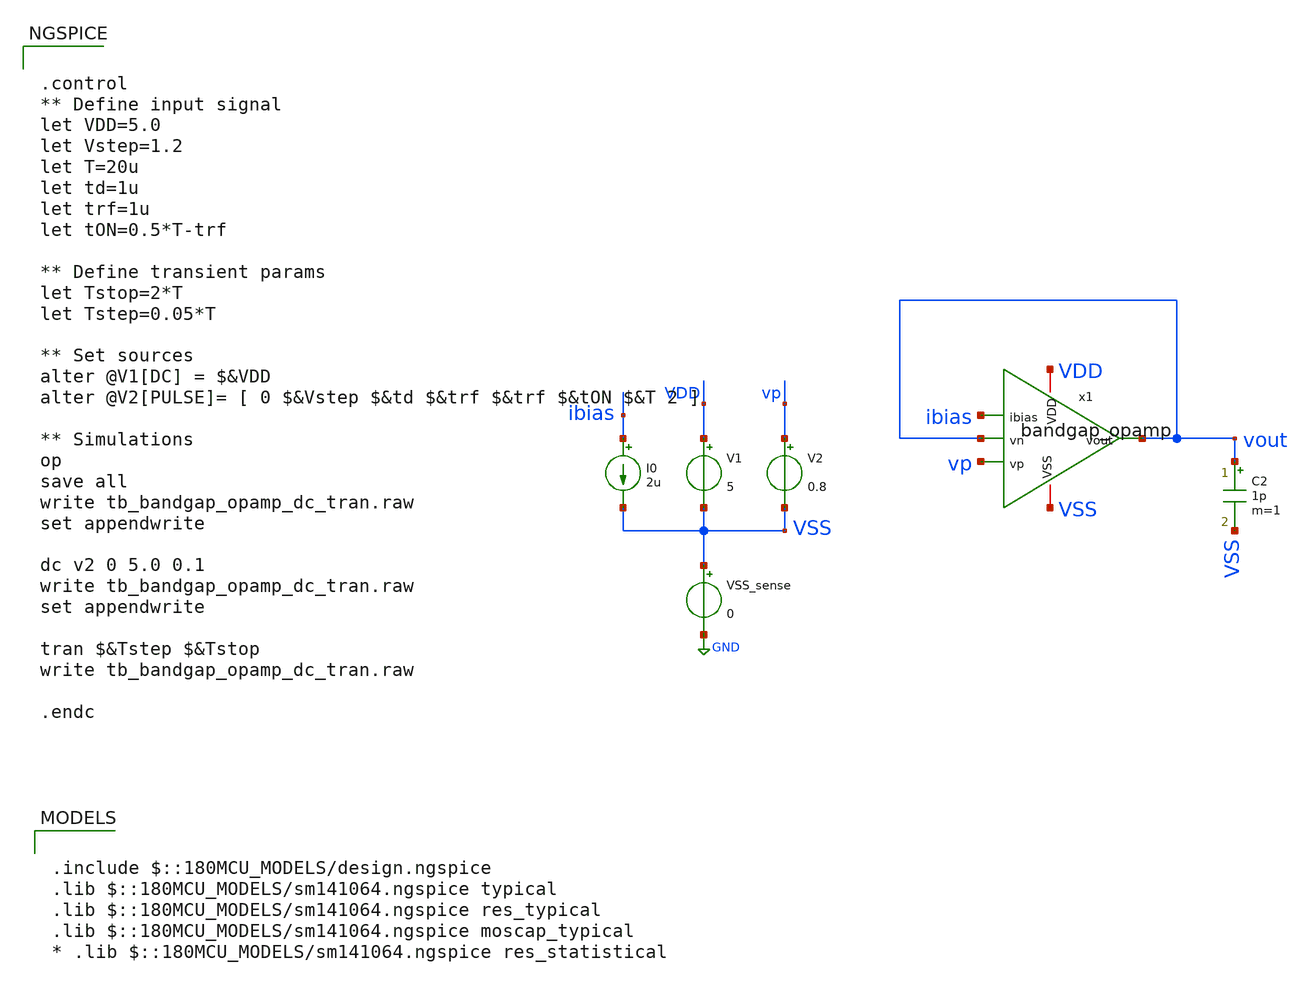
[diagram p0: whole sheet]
** sch_path: designs/libs/tb_bandgap/tb_bandgap_opamp_dc_tran/tb_bandgap_opamp_dc_tran.sch
**.subckt tb_bandgap_opamp_dc_tran
V1 VDD VSS 5
V2 vp VSS 0.8
VSS_sense VSS GND 0
C2 vout VSS 1p m=1
I0 ibias VSS 2u
x1 VDD ibias vout vp vout VSS bandgap_opamp
**** begin user architecture code

.include $::180MCU_MODELS/design.ngspice
.lib $::180MCU_MODELS/sm141064.ngspice typical
.lib $::180MCU_MODELS/sm141064.ngspice res_typical
.lib $::180MCU_MODELS/sm141064.ngspice moscap_typical
* .lib $::180MCU_MODELS/sm141064.ngspice res_statistical



.control
** Define input signal
let VDD=5.0
let Vstep=1.2
let T=20u
let td=1u
let trf=1u
let tON=0.5*T-trf

** Define transient params
let Tstop=2*T
let Tstep=0.05*T

** Set sources
alter @V1[DC] = $&VDD
alter @V2[PULSE]= [ 0 $&Vstep $&td $&trf $&trf $&tON $&T 2 ]

** Simulations
op
save all
write tb_bandgap_opamp_dc_tran.raw
set appendwrite

dc v2 0 5.0 0.1
write tb_bandgap_opamp_dc_tran.raw
set appendwrite

tran $&Tstep $&Tstop
write tb_bandgap_opamp_dc_tran.raw

.endc


**** end user architecture code
**.ends

* expanding   symbol:  libs/core_bandgap/bandgap_opamp/bandgap_opamp.sym # of pins=6
** sym_path: designs/libs/core_bandgap/bandgap_opamp/bandgap_opamp.sym
** sch_path: designs/libs/core_bandgap/bandgap_opamp/bandgap_opamp.sch
.subckt bandgap_opamp VDD ibias vn vp vout VSS
*.ipin vn
*.ipin vp
*.opin vout
*.ipin ibias
*.iopin VDD
*.iopin VSS
XC1 vout net3 cap_nmos_03v3_b c_width=15u c_length=15u m=1
XM9 ibias ibias VDD VDD pfet_05v0 L=1u W=1u nf=1 ad='int((nf+1)/2) * W/nf * 0.18u' as='int((nf+2)/2) * W/nf * 0.18u'
+ pd='2*int((nf+1)/2) * (W/nf + 0.18u)' ps='2*int((nf+2)/2) * (W/nf + 0.18u)' nrd='0.18u / W' nrs='0.18u / W'
+ sa=0 sb=0 sd=0 m=1
XM10 net2 net2 VSS VSS nfet_05v0 L=2u W=1u nf=1 ad='int((nf+1)/2) * W/nf * 0.18u' as='int((nf+2)/2) * W/nf * 0.18u'
+ pd='2*int((nf+1)/2) * (W/nf + 0.18u)' ps='2*int((nf+2)/2) * (W/nf + 0.18u)' nrd='0.18u / W' nrs='0.18u / W'
+ sa=0 sb=0 sd=0 m=1
XM3 net1 ibias VDD VDD pfet_05v0 L=1u W=1u nf=1 ad='int((nf+1)/2) * W/nf * 0.18u' as='int((nf+2)/2) * W/nf * 0.18u'
+ pd='2*int((nf+1)/2) * (W/nf + 0.18u)' ps='2*int((nf+2)/2) * (W/nf + 0.18u)' nrd='0.18u / W' nrs='0.18u / W'
+ sa=0 sb=0 sd=0 m=1
XM4 vout ibias VDD VDD pfet_05v0 L=1u W=1u nf=1 ad='int((nf+1)/2) * W/nf * 0.18u' as='int((nf+2)/2) * W/nf * 0.18u'
+ pd='2*int((nf+1)/2) * (W/nf + 0.18u)' ps='2*int((nf+2)/2) * (W/nf + 0.18u)' nrd='0.18u / W' nrs='0.18u / W'
+ sa=0 sb=0 sd=0 m=4
XM1 net2 vn net1 VDD pfet_05v0 L=1u W=4u nf=1 ad='int((nf+1)/2) * W/nf * 0.18u' as='int((nf+2)/2) * W/nf * 0.18u'
+ pd='2*int((nf+1)/2) * (W/nf + 0.18u)' ps='2*int((nf+2)/2) * (W/nf + 0.18u)' nrd='0.18u / W' nrs='0.18u / W'
+ sa=0 sb=0 sd=0 m=1
XM2 net3 vp net1 VDD pfet_05v0 L=1u W=4u nf=1 ad='int((nf+1)/2) * W/nf * 0.18u' as='int((nf+2)/2) * W/nf * 0.18u'
+ pd='2*int((nf+1)/2) * (W/nf + 0.18u)' ps='2*int((nf+2)/2) * (W/nf + 0.18u)' nrd='0.18u / W' nrs='0.18u / W'
+ sa=0 sb=0 sd=0 m=1
XM5 net3 net2 VSS VSS nfet_05v0 L=2u W=1u nf=1 ad='int((nf+1)/2) * W/nf * 0.18u' as='int((nf+2)/2) * W/nf * 0.18u'
+ pd='2*int((nf+1)/2) * (W/nf + 0.18u)' ps='2*int((nf+2)/2) * (W/nf + 0.18u)' nrd='0.18u / W' nrs='0.18u / W'
+ sa=0 sb=0 sd=0 m=1
XM6 vout net3 VSS VSS nfet_05v0 L=2u W=1u nf=1 ad='int((nf+1)/2) * W/nf * 0.18u' as='int((nf+2)/2) * W/nf * 0.18u'
+ pd='2*int((nf+1)/2) * (W/nf + 0.18u)' ps='2*int((nf+2)/2) * (W/nf + 0.18u)' nrd='0.18u / W' nrs='0.18u / W'
+ sa=0 sb=0 sd=0 m=8
.ends

.GLOBAL GND
.end
